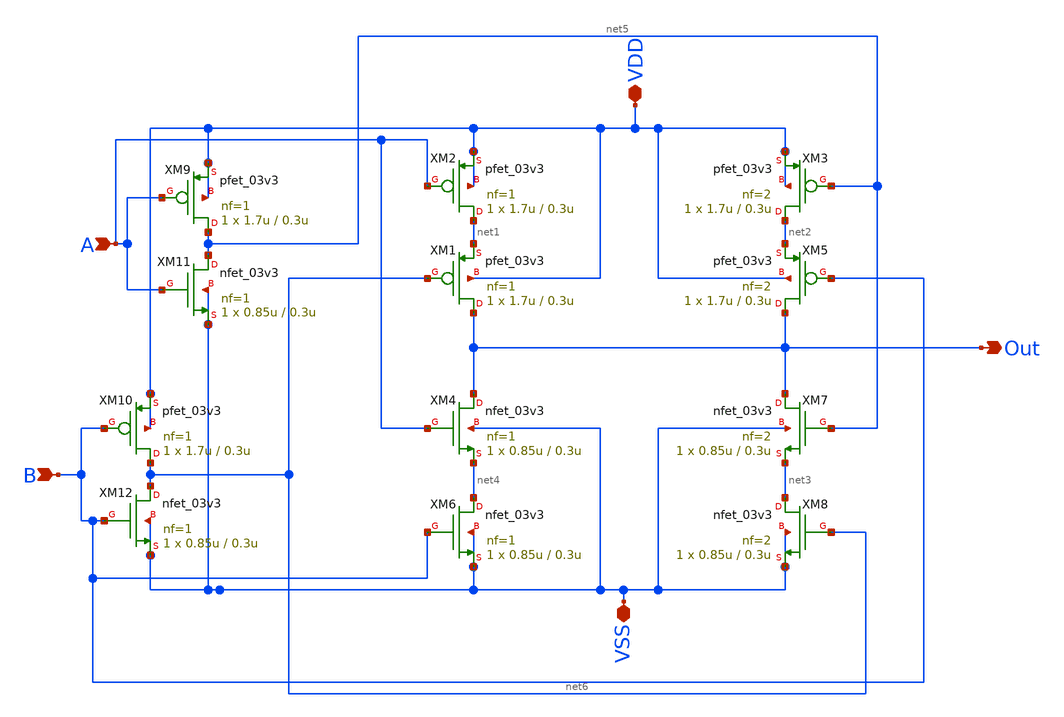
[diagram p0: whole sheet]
** sch_path: cells/comp4/2x_drive/schematic/my_xor_2x.sch
**.subckt my_xor_2x VDD VSS A B Out
*.iopin VDD
*.iopin VSS
*.ipin A
*.ipin B
*.opin Out
XM2 net1 A VDD VDD pfet_03v3 L=0.3u W=1.7u nf=1 ad='int((nf+1)/2) * W/nf * 0.18u' as='int((nf+2)/2) * W/nf * 0.18u'
+ pd='2*int((nf+1)/2) * (W/nf + 0.18u)' ps='2*int((nf+2)/2) * (W/nf + 0.18u)' nrd='0.18u / W' nrs='0.18u / W'
+ sa=0 sb=0 sd=0 m=1
XM4 Out A net4 VSS nfet_03v3 L=0.3u W=0.85u nf=1 ad='int((nf+1)/2) * W/nf * 0.18u' as='int((nf+2)/2) * W/nf * 0.18u'
+ pd='2*int((nf+1)/2) * (W/nf + 0.18u)' ps='2*int((nf+2)/2) * (W/nf + 0.18u)' nrd='0.18u / W' nrs='0.18u / W'
+ sa=0 sb=0 sd=0 m=1
XM1 Out net6 net1 VDD pfet_03v3 L=0.3u W=1.7u nf=1 ad='int((nf+1)/2) * W/nf * 0.18u' as='int((nf+2)/2) * W/nf * 0.18u'
+ pd='2*int((nf+1)/2) * (W/nf + 0.18u)' ps='2*int((nf+2)/2) * (W/nf + 0.18u)' nrd='0.18u / W' nrs='0.18u / W'
+ sa=0 sb=0 sd=0 m=1
XM3 net2 net5 VDD VDD pfet_03v3 L=0.3u W=1.7u nf=2 ad='int((nf+1)/2) * W/nf * 0.18u' as='int((nf+2)/2) * W/nf * 0.18u'
+ pd='2*int((nf+1)/2) * (W/nf + 0.18u)' ps='2*int((nf+2)/2) * (W/nf + 0.18u)' nrd='0.18u / W' nrs='0.18u / W'
+ sa=0 sb=0 sd=0 m=1
XM5 Out B net2 VDD pfet_03v3 L=0.3u W=1.7u nf=2 ad='int((nf+1)/2) * W/nf * 0.18u' as='int((nf+2)/2) * W/nf * 0.18u'
+ pd='2*int((nf+1)/2) * (W/nf + 0.18u)' ps='2*int((nf+2)/2) * (W/nf + 0.18u)' nrd='0.18u / W' nrs='0.18u / W'
+ sa=0 sb=0 sd=0 m=1
XM6 net4 B VSS VSS nfet_03v3 L=0.3u W=0.85u nf=1 ad='int((nf+1)/2) * W/nf * 0.18u' as='int((nf+2)/2) * W/nf * 0.18u'
+ pd='2*int((nf+1)/2) * (W/nf + 0.18u)' ps='2*int((nf+2)/2) * (W/nf + 0.18u)' nrd='0.18u / W' nrs='0.18u / W'
+ sa=0 sb=0 sd=0 m=1
XM7 Out net5 net3 VSS nfet_03v3 L=0.3u W=0.85u nf=2 ad='int((nf+1)/2) * W/nf * 0.18u' as='int((nf+2)/2) * W/nf * 0.18u'
+ pd='2*int((nf+1)/2) * (W/nf + 0.18u)' ps='2*int((nf+2)/2) * (W/nf + 0.18u)' nrd='0.18u / W' nrs='0.18u / W'
+ sa=0 sb=0 sd=0 m=1
XM8 net3 net6 VSS VSS nfet_03v3 L=0.3u W=0.85u nf=2 ad='int((nf+1)/2) * W/nf * 0.18u' as='int((nf+2)/2) * W/nf * 0.18u'
+ pd='2*int((nf+1)/2) * (W/nf + 0.18u)' ps='2*int((nf+2)/2) * (W/nf + 0.18u)' nrd='0.18u / W' nrs='0.18u / W'
+ sa=0 sb=0 sd=0 m=1
XM9 net5 A VDD VDD pfet_03v3 L=0.3u W=1.7u nf=1 ad='int((nf+1)/2) * W/nf * 0.18u' as='int((nf+2)/2) * W/nf * 0.18u'
+ pd='2*int((nf+1)/2) * (W/nf + 0.18u)' ps='2*int((nf+2)/2) * (W/nf + 0.18u)' nrd='0.18u / W' nrs='0.18u / W'
+ sa=0 sb=0 sd=0 m=1
XM10 net6 B VDD VDD pfet_03v3 L=0.3u W=1.7u nf=1 ad='int((nf+1)/2) * W/nf * 0.18u' as='int((nf+2)/2) * W/nf * 0.18u'
+ pd='2*int((nf+1)/2) * (W/nf + 0.18u)' ps='2*int((nf+2)/2) * (W/nf + 0.18u)' nrd='0.18u / W' nrs='0.18u / W'
+ sa=0 sb=0 sd=0 m=1
XM11 net5 A VSS VSS nfet_03v3 L=0.3u W=0.85u nf=1 ad='int((nf+1)/2) * W/nf * 0.18u' as='int((nf+2)/2) * W/nf * 0.18u'
+ pd='2*int((nf+1)/2) * (W/nf + 0.18u)' ps='2*int((nf+2)/2) * (W/nf + 0.18u)' nrd='0.18u / W' nrs='0.18u / W'
+ sa=0 sb=0 sd=0 m=1
XM12 net6 B VSS VSS nfet_03v3 L=0.3u W=0.85u nf=1 ad='int((nf+1)/2) * W/nf * 0.18u' as='int((nf+2)/2) * W/nf * 0.18u'
+ pd='2*int((nf+1)/2) * (W/nf + 0.18u)' ps='2*int((nf+2)/2) * (W/nf + 0.18u)' nrd='0.18u / W' nrs='0.18u / W'
+ sa=0 sb=0 sd=0 m=1
**.ends
.end
